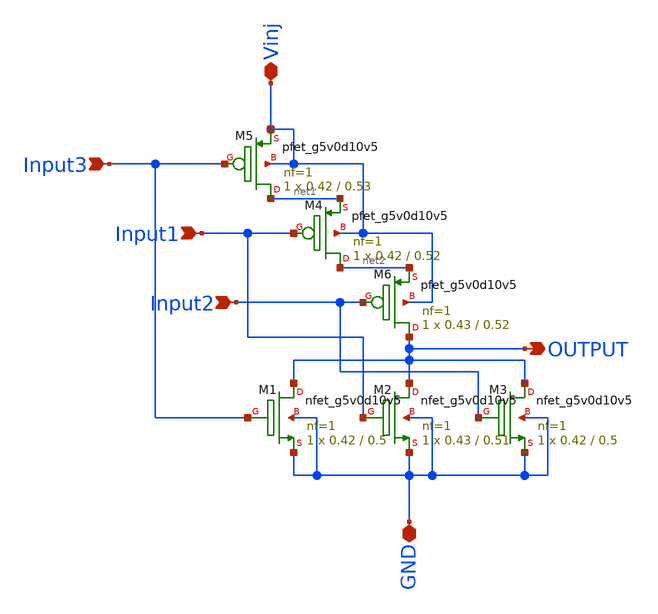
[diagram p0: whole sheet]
** sch_path: sky130_cells/RDAC/Design/sky130_hilas_VinjNOR3.sch
**.subckt sky130_hilas_VinjNOR3 Input3 Input1 Input2 Vinj GND OUTPUT
*.ipin Input3
*.ipin Input1
*.ipin Input2
*.iopin Vinj
*.iopin GND
*.opin OUTPUT
XM1 OUTPUT Input3 GND GND sky130_fd_pr__nfet_g5v0d10v5 L=0.5 W=0.42 nf=1 ad='int((nf+1)/2) * W/nf * 0.29'
+ as='int((nf+2)/2) * W/nf * 0.29' pd='2*int((nf+1)/2) * (W/nf + 0.29)' ps='2*int((nf+2)/2) * (W/nf + 0.29)'
+ nrd='0.29 / W' nrs='0.29 / W' sa=0 sb=0 sd=0 mult=1 m=1
XM2 OUTPUT Input1 GND GND sky130_fd_pr__nfet_g5v0d10v5 L=0.51 W=0.43 nf=1 ad='int((nf+1)/2) * W/nf * 0.29'
+ as='int((nf+2)/2) * W/nf * 0.29' pd='2*int((nf+1)/2) * (W/nf + 0.29)' ps='2*int((nf+2)/2) * (W/nf + 0.29)'
+ nrd='0.29 / W' nrs='0.29 / W' sa=0 sb=0 sd=0 mult=1 m=1
XM3 OUTPUT Input2 GND GND sky130_fd_pr__nfet_g5v0d10v5 L=0.5 W=0.42 nf=1 ad='int((nf+1)/2) * W/nf * 0.29'
+ as='int((nf+2)/2) * W/nf * 0.29' pd='2*int((nf+1)/2) * (W/nf + 0.29)' ps='2*int((nf+2)/2) * (W/nf + 0.29)'
+ nrd='0.29 / W' nrs='0.29 / W' sa=0 sb=0 sd=0 mult=1 m=1
XM6 OUTPUT Input2 net2 Vinj sky130_fd_pr__pfet_g5v0d10v5 L=0.52 W=0.43 nf=1 ad='int((nf+1)/2) * W/nf * 0.29'
+ as='int((nf+2)/2) * W/nf * 0.29' pd='2*int((nf+1)/2) * (W/nf + 0.29)' ps='2*int((nf+2)/2) * (W/nf + 0.29)'
+ nrd='0.29 / W' nrs='0.29 / W' sa=0 sb=0 sd=0 mult=1 m=1
XM4 net2 Input1 net1 Vinj sky130_fd_pr__pfet_g5v0d10v5 L=0.52 W=0.42 nf=1 ad='int((nf+1)/2) * W/nf * 0.29'
+ as='int((nf+2)/2) * W/nf * 0.29' pd='2*int((nf+1)/2) * (W/nf + 0.29)' ps='2*int((nf+2)/2) * (W/nf + 0.29)'
+ nrd='0.29 / W' nrs='0.29 / W' sa=0 sb=0 sd=0 mult=1 m=1
XM5 net1 Input3 Vinj Vinj sky130_fd_pr__pfet_g5v0d10v5 L=0.53 W=0.42 nf=1 ad='int((nf+1)/2) * W/nf * 0.29'
+ as='int((nf+2)/2) * W/nf * 0.29' pd='2*int((nf+1)/2) * (W/nf + 0.29)' ps='2*int((nf+2)/2) * (W/nf + 0.29)'
+ nrd='0.29 / W' nrs='0.29 / W' sa=0 sb=0 sd=0 mult=1 m=1
**.ends
.end
